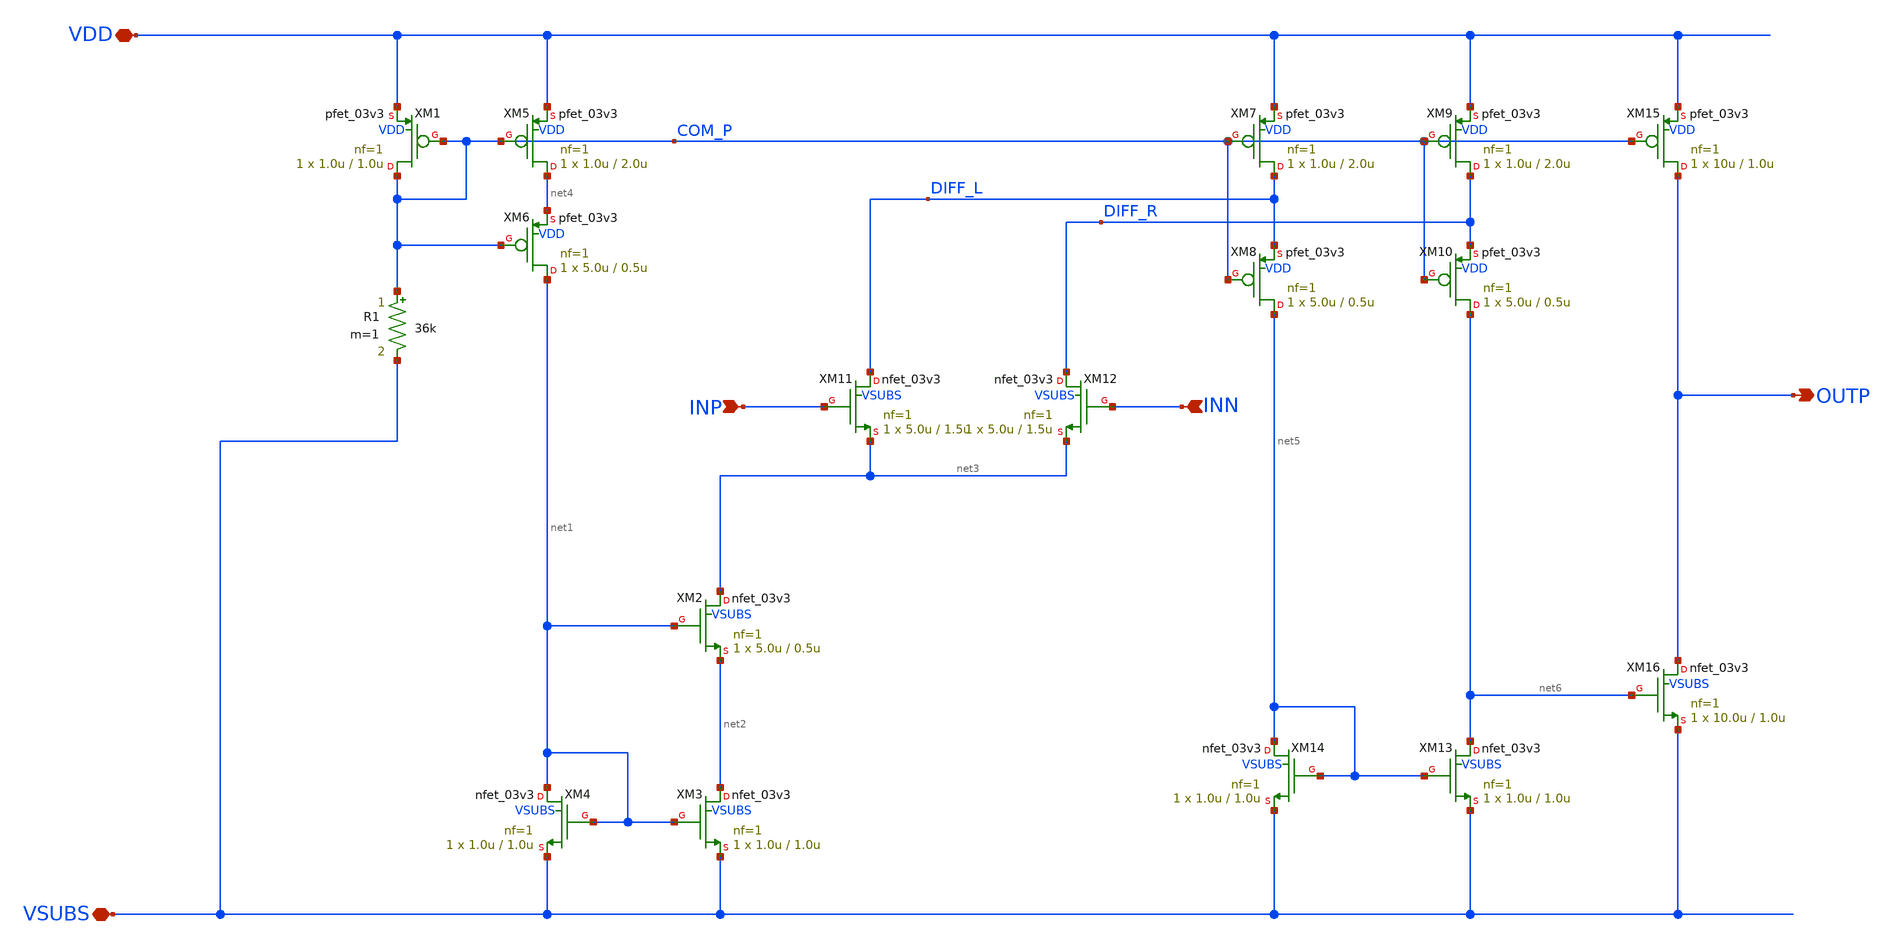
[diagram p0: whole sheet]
** sch_path: xschem/ip_amplifier.sch
**.subckt ip_amplifier VDD VSUBS INP INN OUTP
*.iopin VDD
*.iopin VSUBS
*.ipin INP
*.ipin INN
*.opin OUTP
XM1 COM_P COM_P VDD VDD pfet_03v3 L=1.0u W=1.0u nf=1 ad='int((nf+1)/2) * W/nf * 0.18u' as='int((nf+2)/2) * W/nf * 0.18u'
+ pd='2*int((nf+1)/2) * (W/nf + 0.18u)' ps='2*int((nf+2)/2) * (W/nf + 0.18u)' nrd='0.18u / W' nrs='0.18u / W'
+ sa=0 sb=0 sd=0 m=1 par=1
XM2 net3 net1 net2 VSUBS nfet_03v3 L=0.5u W=5.0u nf=1 ad='int((nf+1)/2) * W/nf * 0.18u' as='int((nf+2)/2) * W/nf * 0.18u'
+ pd='2*int((nf+1)/2) * (W/nf + 0.18u)' ps='2*int((nf+2)/2) * (W/nf + 0.18u)' nrd='0.18u / W' nrs='0.18u / W'
+ sa=0 sb=0 sd=0 m=1 par=1
XM3 net2 net1 VSUBS VSUBS nfet_03v3 L=1.0u W=1.0u nf=1 ad='int((nf+1)/2) * W/nf * 0.18u' as='int((nf+2)/2) * W/nf * 0.18u'
+ pd='2*int((nf+1)/2) * (W/nf + 0.18u)' ps='2*int((nf+2)/2) * (W/nf + 0.18u)' nrd='0.18u / W' nrs='0.18u / W'
+ sa=0 sb=0 sd=0 m=1 par=1
XM4 net1 net1 VSUBS VSUBS nfet_03v3 L=1.0u W=1.0u nf=1 ad='int((nf+1)/2) * W/nf * 0.18u' as='int((nf+2)/2) * W/nf * 0.18u'
+ pd='2*int((nf+1)/2) * (W/nf + 0.18u)' ps='2*int((nf+2)/2) * (W/nf + 0.18u)' nrd='0.18u / W' nrs='0.18u / W'
+ sa=0 sb=0 sd=0 m=1 par=1
XM5 net4 COM_P VDD VDD pfet_03v3 L=2.0u W=1.0u nf=1 ad='int((nf+1)/2) * W/nf * 0.18u' as='int((nf+2)/2) * W/nf * 0.18u'
+ pd='2*int((nf+1)/2) * (W/nf + 0.18u)' ps='2*int((nf+2)/2) * (W/nf + 0.18u)' nrd='0.18u / W' nrs='0.18u / W'
+ sa=0 sb=0 sd=0 m=1 par=1
XM6 net1 COM_P net4 VDD pfet_03v3 L=0.5u W=5.0u nf=1 ad='int((nf+1)/2) * W/nf * 0.18u' as='int((nf+2)/2) * W/nf * 0.18u'
+ pd='2*int((nf+1)/2) * (W/nf + 0.18u)' ps='2*int((nf+2)/2) * (W/nf + 0.18u)' nrd='0.18u / W' nrs='0.18u / W'
+ sa=0 sb=0 sd=0 m=1 par=1
XM7 DIFF_L COM_P VDD VDD pfet_03v3 L=2.0u W=1.0u nf=1 ad='int((nf+1)/2) * W/nf * 0.18u' as='int((nf+2)/2) * W/nf * 0.18u'
+ pd='2*int((nf+1)/2) * (W/nf + 0.18u)' ps='2*int((nf+2)/2) * (W/nf + 0.18u)' nrd='0.18u / W' nrs='0.18u / W'
+ sa=0 sb=0 sd=0 m=1 par=1
XM9 DIFF_R COM_P VDD VDD pfet_03v3 L=2.0u W=1.0u nf=1 ad='int((nf+1)/2) * W/nf * 0.18u' as='int((nf+2)/2) * W/nf * 0.18u'
+ pd='2*int((nf+1)/2) * (W/nf + 0.18u)' ps='2*int((nf+2)/2) * (W/nf + 0.18u)' nrd='0.18u / W' nrs='0.18u / W'
+ sa=0 sb=0 sd=0 m=1 par=1
XM11 DIFF_L INP net3 VSUBS nfet_03v3 L=1.5u W=5.0u nf=1 ad='int((nf+1)/2) * W/nf * 0.18u' as='int((nf+2)/2) * W/nf * 0.18u'
+ pd='2*int((nf+1)/2) * (W/nf + 0.18u)' ps='2*int((nf+2)/2) * (W/nf + 0.18u)' nrd='0.18u / W' nrs='0.18u / W'
+ sa=0 sb=0 sd=0 m=1 par=1
XM12 DIFF_R INN net3 VSUBS nfet_03v3 L=1.5u W=5.0u nf=1 ad='int((nf+1)/2) * W/nf * 0.18u' as='int((nf+2)/2) * W/nf * 0.18u'
+ pd='2*int((nf+1)/2) * (W/nf + 0.18u)' ps='2*int((nf+2)/2) * (W/nf + 0.18u)' nrd='0.18u / W' nrs='0.18u / W'
+ sa=0 sb=0 sd=0 m=1 par=1
XM8 net5 COM_P DIFF_L VDD pfet_03v3 L=0.5u W=5.0u nf=1 ad='int((nf+1)/2) * W/nf * 0.18u' as='int((nf+2)/2) * W/nf * 0.18u'
+ pd='2*int((nf+1)/2) * (W/nf + 0.18u)' ps='2*int((nf+2)/2) * (W/nf + 0.18u)' nrd='0.18u / W' nrs='0.18u / W'
+ sa=0 sb=0 sd=0 m=1 par=1
XM10 net6 COM_P DIFF_R VDD pfet_03v3 L=0.5u W=5.0u nf=1 ad='int((nf+1)/2) * W/nf * 0.18u' as='int((nf+2)/2) * W/nf * 0.18u'
+ pd='2*int((nf+1)/2) * (W/nf + 0.18u)' ps='2*int((nf+2)/2) * (W/nf + 0.18u)' nrd='0.18u / W' nrs='0.18u / W'
+ sa=0 sb=0 sd=0 m=1 par=1
XM13 net6 net5 VSUBS VSUBS nfet_03v3 L=1.0u W=1.0u nf=1 ad='int((nf+1)/2) * W/nf * 0.18u' as='int((nf+2)/2) * W/nf * 0.18u'
+ pd='2*int((nf+1)/2) * (W/nf + 0.18u)' ps='2*int((nf+2)/2) * (W/nf + 0.18u)' nrd='0.18u / W' nrs='0.18u / W'
+ sa=0 sb=0 sd=0 m=1 par=1
XM14 net5 net5 VSUBS VSUBS nfet_03v3 L=1.0u W=1.0u nf=1 ad='int((nf+1)/2) * W/nf * 0.18u' as='int((nf+2)/2) * W/nf * 0.18u'
+ pd='2*int((nf+1)/2) * (W/nf + 0.18u)' ps='2*int((nf+2)/2) * (W/nf + 0.18u)' nrd='0.18u / W' nrs='0.18u / W'
+ sa=0 sb=0 sd=0 m=1 par=1
XM15 OUTP COM_P VDD VDD pfet_03v3 L=1.0u W=10u nf=1 ad='int((nf+1)/2) * W/nf * 0.18u' as='int((nf+2)/2) * W/nf * 0.18u'
+ pd='2*int((nf+1)/2) * (W/nf + 0.18u)' ps='2*int((nf+2)/2) * (W/nf + 0.18u)' nrd='0.18u / W' nrs='0.18u / W'
+ sa=0 sb=0 sd=0 m=1 par=1
XM16 OUTP net6 VSUBS VSUBS nfet_03v3 L=1.0u W=10.0u nf=1 ad='int((nf+1)/2) * W/nf * 0.18u' as='int((nf+2)/2) * W/nf * 0.18u'
+ pd='2*int((nf+1)/2) * (W/nf + 0.18u)' ps='2*int((nf+2)/2) * (W/nf + 0.18u)' nrd='0.18u / W' nrs='0.18u / W'
+ sa=0 sb=0 sd=0 m=1 par=1
R1 COM_P VSUBS 36k m=1
**.ends
.end
